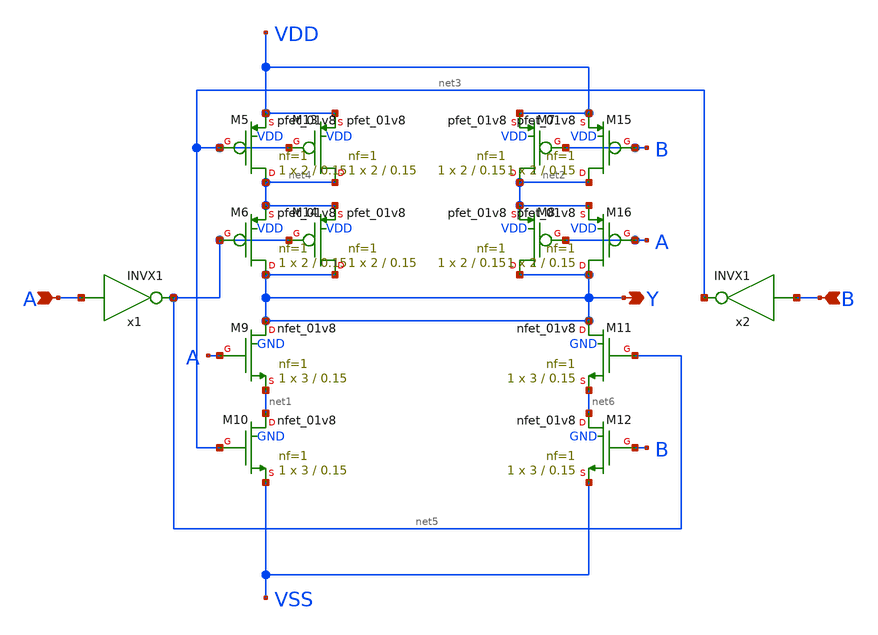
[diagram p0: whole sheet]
** sch_path: lib/xschem/XNOR2X1.sch
**.subckt XNOR2X1 A Y B
*.ipin A
*.opin Y
*.ipin B
XM5 net4 net3 VDD VDD sky130_fd_pr__pfet_01v8 L=0.15 W=2 nf=1 ad='int((nf+1)/2) * W/nf * 0.29' as='int((nf+2)/2) * W/nf * 0.29'
+ pd='2*int((nf+1)/2) * (W/nf + 0.29)' ps='2*int((nf+2)/2) * (W/nf + 0.29)' nrd='0.29 / W' nrs='0.29 / W'
+ sa=0 sb=0 sd=0 mult=1 m=1
XM6 Y net5 net4 VDD sky130_fd_pr__pfet_01v8 L=0.15 W=2 nf=1 ad='int((nf+1)/2) * W/nf * 0.29' as='int((nf+2)/2) * W/nf * 0.29'
+ pd='2*int((nf+1)/2) * (W/nf + 0.29)' ps='2*int((nf+2)/2) * (W/nf + 0.29)' nrd='0.29 / W' nrs='0.29 / W'
+ sa=0 sb=0 sd=0 mult=1 m=1
XM7 net2 B VDD VDD sky130_fd_pr__pfet_01v8 L=0.15 W=2 nf=1 ad='int((nf+1)/2) * W/nf * 0.29' as='int((nf+2)/2) * W/nf * 0.29'
+ pd='2*int((nf+1)/2) * (W/nf + 0.29)' ps='2*int((nf+2)/2) * (W/nf + 0.29)' nrd='0.29 / W' nrs='0.29 / W'
+ sa=0 sb=0 sd=0 mult=1 m=1
XM8 Y A net2 VDD sky130_fd_pr__pfet_01v8 L=0.15 W=2 nf=1 ad='int((nf+1)/2) * W/nf * 0.29' as='int((nf+2)/2) * W/nf * 0.29'
+ pd='2*int((nf+1)/2) * (W/nf + 0.29)' ps='2*int((nf+2)/2) * (W/nf + 0.29)' nrd='0.29 / W' nrs='0.29 / W'
+ sa=0 sb=0 sd=0 mult=1 m=1
XM9 Y A net1 GND sky130_fd_pr__nfet_01v8 L=0.15 W=3 nf=1 ad='int((nf+1)/2) * W/nf * 0.29' as='int((nf+2)/2) * W/nf * 0.29'
+ pd='2*int((nf+1)/2) * (W/nf + 0.29)' ps='2*int((nf+2)/2) * (W/nf + 0.29)' nrd='0.29 / W' nrs='0.29 / W'
+ sa=0 sb=0 sd=0 mult=1 m=1
XM10 net1 net3 VSS GND sky130_fd_pr__nfet_01v8 L=0.15 W=3 nf=1 ad='int((nf+1)/2) * W/nf * 0.29' as='int((nf+2)/2) * W/nf * 0.29'
+ pd='2*int((nf+1)/2) * (W/nf + 0.29)' ps='2*int((nf+2)/2) * (W/nf + 0.29)' nrd='0.29 / W' nrs='0.29 / W'
+ sa=0 sb=0 sd=0 mult=1 m=1
XM11 Y net5 net6 GND sky130_fd_pr__nfet_01v8 L=0.15 W=3 nf=1 ad='int((nf+1)/2) * W/nf * 0.29' as='int((nf+2)/2) * W/nf * 0.29'
+ pd='2*int((nf+1)/2) * (W/nf + 0.29)' ps='2*int((nf+2)/2) * (W/nf + 0.29)' nrd='0.29 / W' nrs='0.29 / W'
+ sa=0 sb=0 sd=0 mult=1 m=1
XM12 net6 B VSS GND sky130_fd_pr__nfet_01v8 L=0.15 W=3 nf=1 ad='int((nf+1)/2) * W/nf * 0.29' as='int((nf+2)/2) * W/nf * 0.29'
+ pd='2*int((nf+1)/2) * (W/nf + 0.29)' ps='2*int((nf+2)/2) * (W/nf + 0.29)' nrd='0.29 / W' nrs='0.29 / W'
+ sa=0 sb=0 sd=0 mult=1 m=1
XM13 net4 net3 VDD VDD sky130_fd_pr__pfet_01v8 L=0.15 W=2 nf=1 ad='int((nf+1)/2) * W/nf * 0.29' as='int((nf+2)/2) * W/nf * 0.29'
+ pd='2*int((nf+1)/2) * (W/nf + 0.29)' ps='2*int((nf+2)/2) * (W/nf + 0.29)' nrd='0.29 / W' nrs='0.29 / W'
+ sa=0 sb=0 sd=0 mult=1 m=1
XM14 Y net5 net4 VDD sky130_fd_pr__pfet_01v8 L=0.15 W=2 nf=1 ad='int((nf+1)/2) * W/nf * 0.29' as='int((nf+2)/2) * W/nf * 0.29'
+ pd='2*int((nf+1)/2) * (W/nf + 0.29)' ps='2*int((nf+2)/2) * (W/nf + 0.29)' nrd='0.29 / W' nrs='0.29 / W'
+ sa=0 sb=0 sd=0 mult=1 m=1
XM15 net2 B VDD VDD sky130_fd_pr__pfet_01v8 L=0.15 W=2 nf=1 ad='int((nf+1)/2) * W/nf * 0.29' as='int((nf+2)/2) * W/nf * 0.29'
+ pd='2*int((nf+1)/2) * (W/nf + 0.29)' ps='2*int((nf+2)/2) * (W/nf + 0.29)' nrd='0.29 / W' nrs='0.29 / W'
+ sa=0 sb=0 sd=0 mult=1 m=1
XM16 Y A net2 VDD sky130_fd_pr__pfet_01v8 L=0.15 W=2 nf=1 ad='int((nf+1)/2) * W/nf * 0.29' as='int((nf+2)/2) * W/nf * 0.29'
+ pd='2*int((nf+1)/2) * (W/nf + 0.29)' ps='2*int((nf+2)/2) * (W/nf + 0.29)' nrd='0.29 / W' nrs='0.29 / W'
+ sa=0 sb=0 sd=0 mult=1 m=1
x1 net5 A INVX1
x2 net3 B INVX1
**.ends
.end
